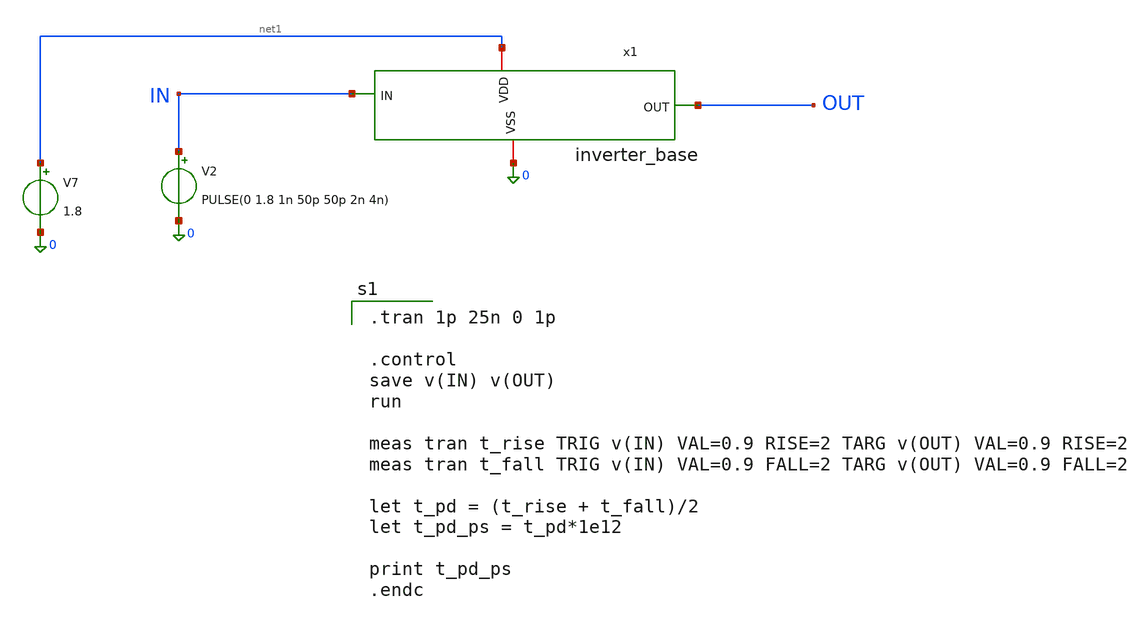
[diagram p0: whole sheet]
** sch_path: xschem/schematic/SCI_DCDL/TG_SCI/TB_inverter_base.sch
**.subckt TB_inverter_base
x1 net1 IN OUT 0 inverter_base
V2 IN 0 PULSE(0 1.8 1n 50p 50p 2n 4n)
V7 net1 0 1.8
**** begin user architecture code

.tran 1p 25n 0 1p

.control
save v(IN) v(OUT)
run

meas tran t_rise TRIG v(IN) VAL=0.9 RISE=2 TARG v(OUT) VAL=0.9 RISE=2
meas tran t_fall TRIG v(IN) VAL=0.9 FALL=2 TARG v(OUT) VAL=0.9 FALL=2

let t_pd = (t_rise + t_fall)/2
let t_pd_ps = t_pd*1e12

print t_pd_ps
.endc



** opencircuitdesign pdks install
.lib $::SKYWATER_MODELS/sky130.lib.spice tt

**** end user architecture code
**.ends
.end
